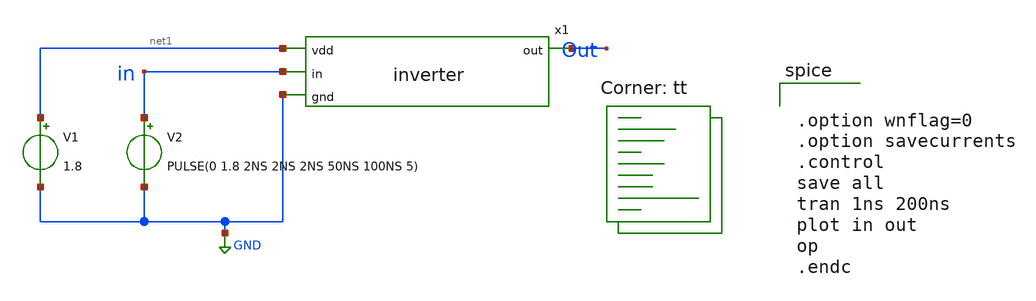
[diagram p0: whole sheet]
** sch_path: oscillator/inverter_tb.sch
**.subckt inverter_tb
x1 net1 in Out GND inverter
V1 net1 GND 1.8
V2 in GND PULSE(0 1.8 2NS 2NS 2NS 50NS 100NS 5)
**** begin user architecture code
.lib $::SKYWATER_MODELS/sky130.lib.spice tt


.option wnflag=0
.option savecurrents
.control
save all
tran 1ns 200ns
plot in out
op
.endc


**** end user architecture code
**.ends

* expanding   symbol:  inverter.sym # of pins=4
** sym_path: oscillator/inverter.sym
** sch_path: oscillator/inverter.sch
.subckt inverter vdd in out gnd
*.ipin vdd
*.ipin in
*.ipin gnd
*.opin out
XM1 out in vdd vdd sky130_fd_pr__pfet_01v8 L=0.15 W=1 nf=1 ad='int((nf+1)/2) * W/nf * 0.29' as='int((nf+2)/2) * W/nf * 0.29'
+ pd='2*int((nf+1)/2) * (W/nf + 0.29)' ps='2*int((nf+2)/2) * (W/nf + 0.29)' nrd='0.29 / W' nrs='0.29 / W'
+ sa=0 sb=0 sd=0 mult=1 m=1
XM2 out in gnd gnd sky130_fd_pr__nfet_01v8 L=0.15 W=1 nf=1 ad='int((nf+1)/2) * W/nf * 0.29' as='int((nf+2)/2) * W/nf * 0.29'
+ pd='2*int((nf+1)/2) * (W/nf + 0.29)' ps='2*int((nf+2)/2) * (W/nf + 0.29)' nrd='0.29 / W' nrs='0.29 / W'
+ sa=0 sb=0 sd=0 mult=1 m=1
.ends

.GLOBAL GND
.end
